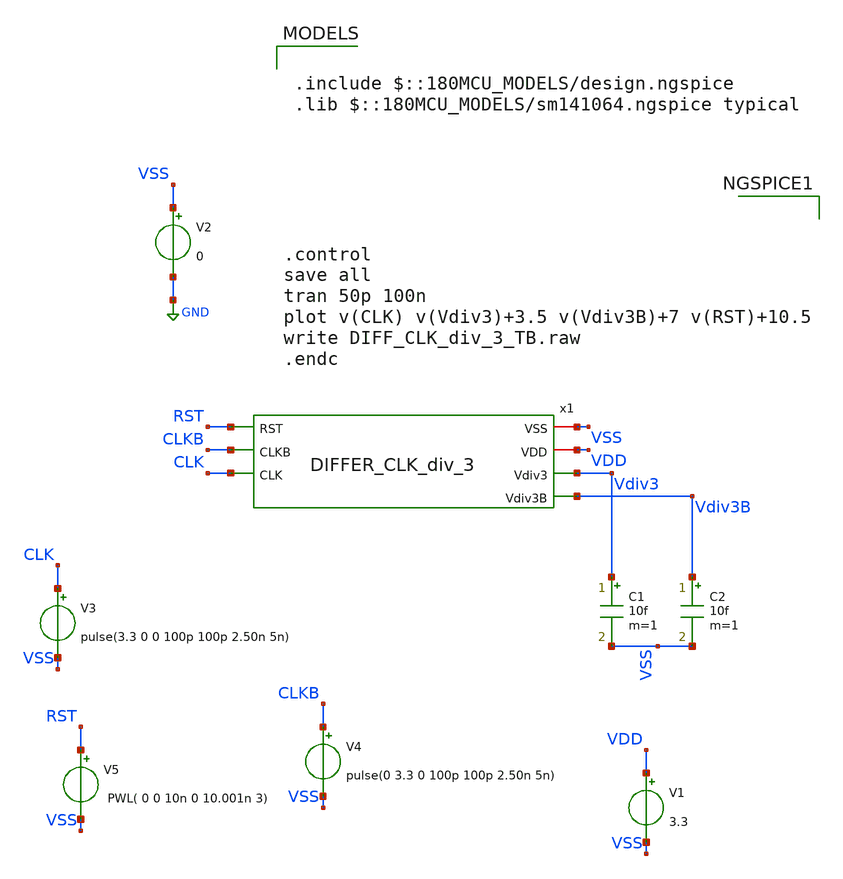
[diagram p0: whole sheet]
** sch_path: Clock_Generator_PAKISTAN_02/Schematics/DIFF_CLK_div_3_TB.sch
**.subckt DIFF_CLK_div_3_TB
V1 VDD VSS 3.3
V2 VSS GND 0
V3 CLK VSS pulse(3.3 0 0 100p 100p 2.50n 5n)
C1 Vdiv3 VSS 10f m=1
C2 Vdiv3B VSS 10f m=1
V5 RST VSS PWL( 0 0 10n 0 10.001n 3)
V4 CLKB VSS pulse(0 3.3 0 100p 100p 2.50n 5n)
x1 VSS VDD RST Vdiv3 Vdiv3B CLKB CLK DIFFER_CLK_div_3
**** begin user architecture code

.include $::180MCU_MODELS/design.ngspice
.lib $::180MCU_MODELS/sm141064.ngspice typical




.control
save all
tran 50p 100n
plot v(CLK) v(Vdiv3)+3.5 v(Vdiv3B)+7 v(RST)+10.5
write DIFF_CLK_div_3_TB.raw
.endc


**** end user architecture code
**.ends
.GLOBAL GND
.end
